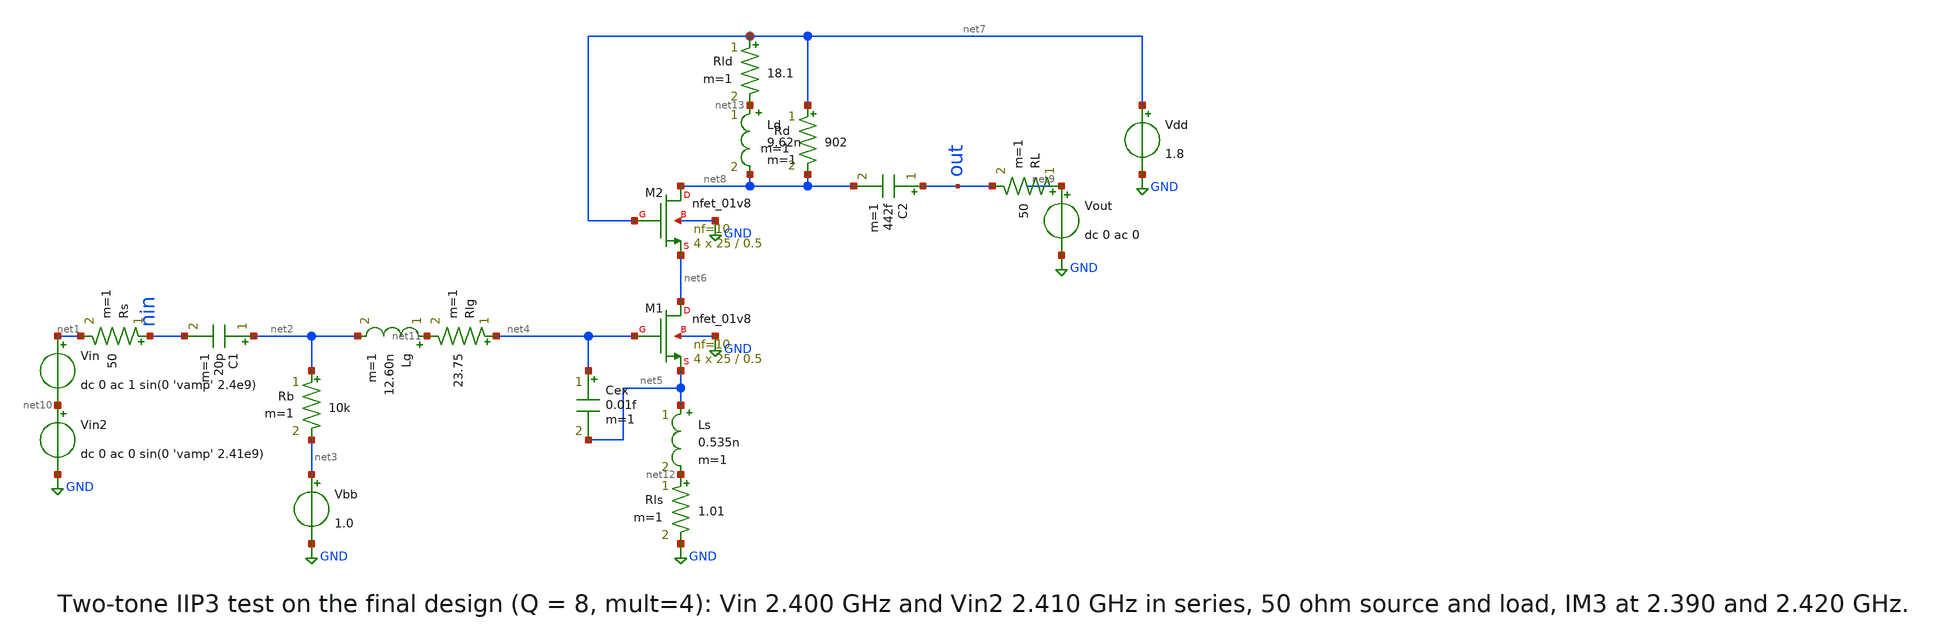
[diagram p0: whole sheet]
** sch_path: 03-sky130-lna-2p4ghz/simulation/lna_twotone_final.sch
**.subckt lna_twotone_final
XM1 net6 net4 net5 GND sky130_fd_pr__nfet_01v8 L=0.5 W=25 nf=10 ad='int((nf+1)/2) * W/nf * 0.29' as='int((nf+2)/2) * W/nf * 0.29'
+ pd='2*int((nf+1)/2) * (W/nf + 0.29)' ps='2*int((nf+2)/2) * (W/nf + 0.29)' nrd='0.29 / W' nrs='0.29 / W'
+ sa=0 sb=0 sd=0 mult=4 m=4
XM2 net8 net7 net6 GND sky130_fd_pr__nfet_01v8 L=0.5 W=25 nf=10 ad='int((nf+1)/2) * W/nf * 0.29' as='int((nf+2)/2) * W/nf * 0.29'
+ pd='2*int((nf+1)/2) * (W/nf + 0.29)' ps='2*int((nf+2)/2) * (W/nf + 0.29)' nrd='0.29 / W' nrs='0.29 / W'
+ sa=0 sb=0 sd=0 mult=4 m=4
Vin net1 net10 dc 0 ac 1 sin(0 'vamp' 2.4e9)
Rs nin net1 50 m=1
C1 net2 nin 20p m=1
Lg net11 net2 12.60n m=1
Rlg net4 net11 23.75 m=1
Rb net2 net3 10k m=1
Vbb net3 GND 1.0
Cex net4 net5 0.01f m=1
Ls net5 net12 0.535n m=1
Rls net12 GND 1.01 m=1
Ld net13 net8 9.62n m=1
Rld net7 net13 18.1 m=1
Rd net7 net8 902 m=1
C2 out net8 442f m=1
RL net9 out 50 m=1
Vout net9 GND dc 0 ac 0
Vdd net7 GND 1.8
Vin2 net10 GND dc 0 ac 0 sin(0 'vamp' 2.41e9)
**** begin user architecture code


.lib /home/nehan/.volare/sky130A/libs.tech/ngspice/sky130.lib.spice tt
.GLOBAL GND
.param vamp=0.0356
.control
save all

* ---- two-tone test: 2.400 and 2.410 GHz, IM3 at 2.390 and 2.420 GHz ----
* window = 100 ns, so every tone fits a whole number of cycles
foreach pdbm -28 -25 -22
  let amp = sqrt(8*50*1e-3*10^($pdbm/10))
  alterparam vamp = $&amp
  reset
  tran 10p 110n 10n 10p
  let ca = v(out)*cos(2*pi*2.39e9*time)
  let sa = v(out)*sin(2*pi*2.39e9*time)
  let cb = v(out)*cos(2*pi*2.40e9*time)
  let sb = v(out)*sin(2*pi*2.40e9*time)
  let cc = v(out)*cos(2*pi*2.41e9*time)
  let sc = v(out)*sin(2*pi*2.41e9*time)
  let cd = v(out)*cos(2*pi*2.42e9*time)
  let sd = v(out)*sin(2*pi*2.42e9*time)
  meas tran mca integ ca from=10n to=110n
  meas tran msa integ sa from=10n to=110n
  meas tran mcb integ cb from=10n to=110n
  meas tran msb integ sb from=10n to=110n
  meas tran mcc integ cc from=10n to=110n
  meas tran msc integ sc from=10n to=110n
  meas tran mcd integ cd from=10n to=110n
  meas tran msd integ sd from=10n to=110n
  let a_a = 2/1e-7*sqrt(mca*mca+msa*msa)
  let a_b = 2/1e-7*sqrt(mcb*mcb+msb*msb)
  let a_c = 2/1e-7*sqrt(mcc*mcc+msc*msc)
  let a_d = 2/1e-7*sqrt(mcd*mcd+msd*msd)
  let af = (a_b + a_c)/2
  let aim = (a_a + a_d)/2
  let pfund = 10*log10(af*af/100/1e-3)
  let delta = 20*log10(af/aim)
  let iip3 = $pdbm + delta/2
  let oip3 = pfund + delta/2
  echo Pin/tone = $pdbm dBm  Pout/tone = $&pfund dBm  IM3 below fundamental = $&delta dB  IIP3 =
+ $&iip3 dBm  OIP3 = $&oip3 dBm
end
.endc


**** end user architecture code
**.ends
.GLOBAL GND
.end
